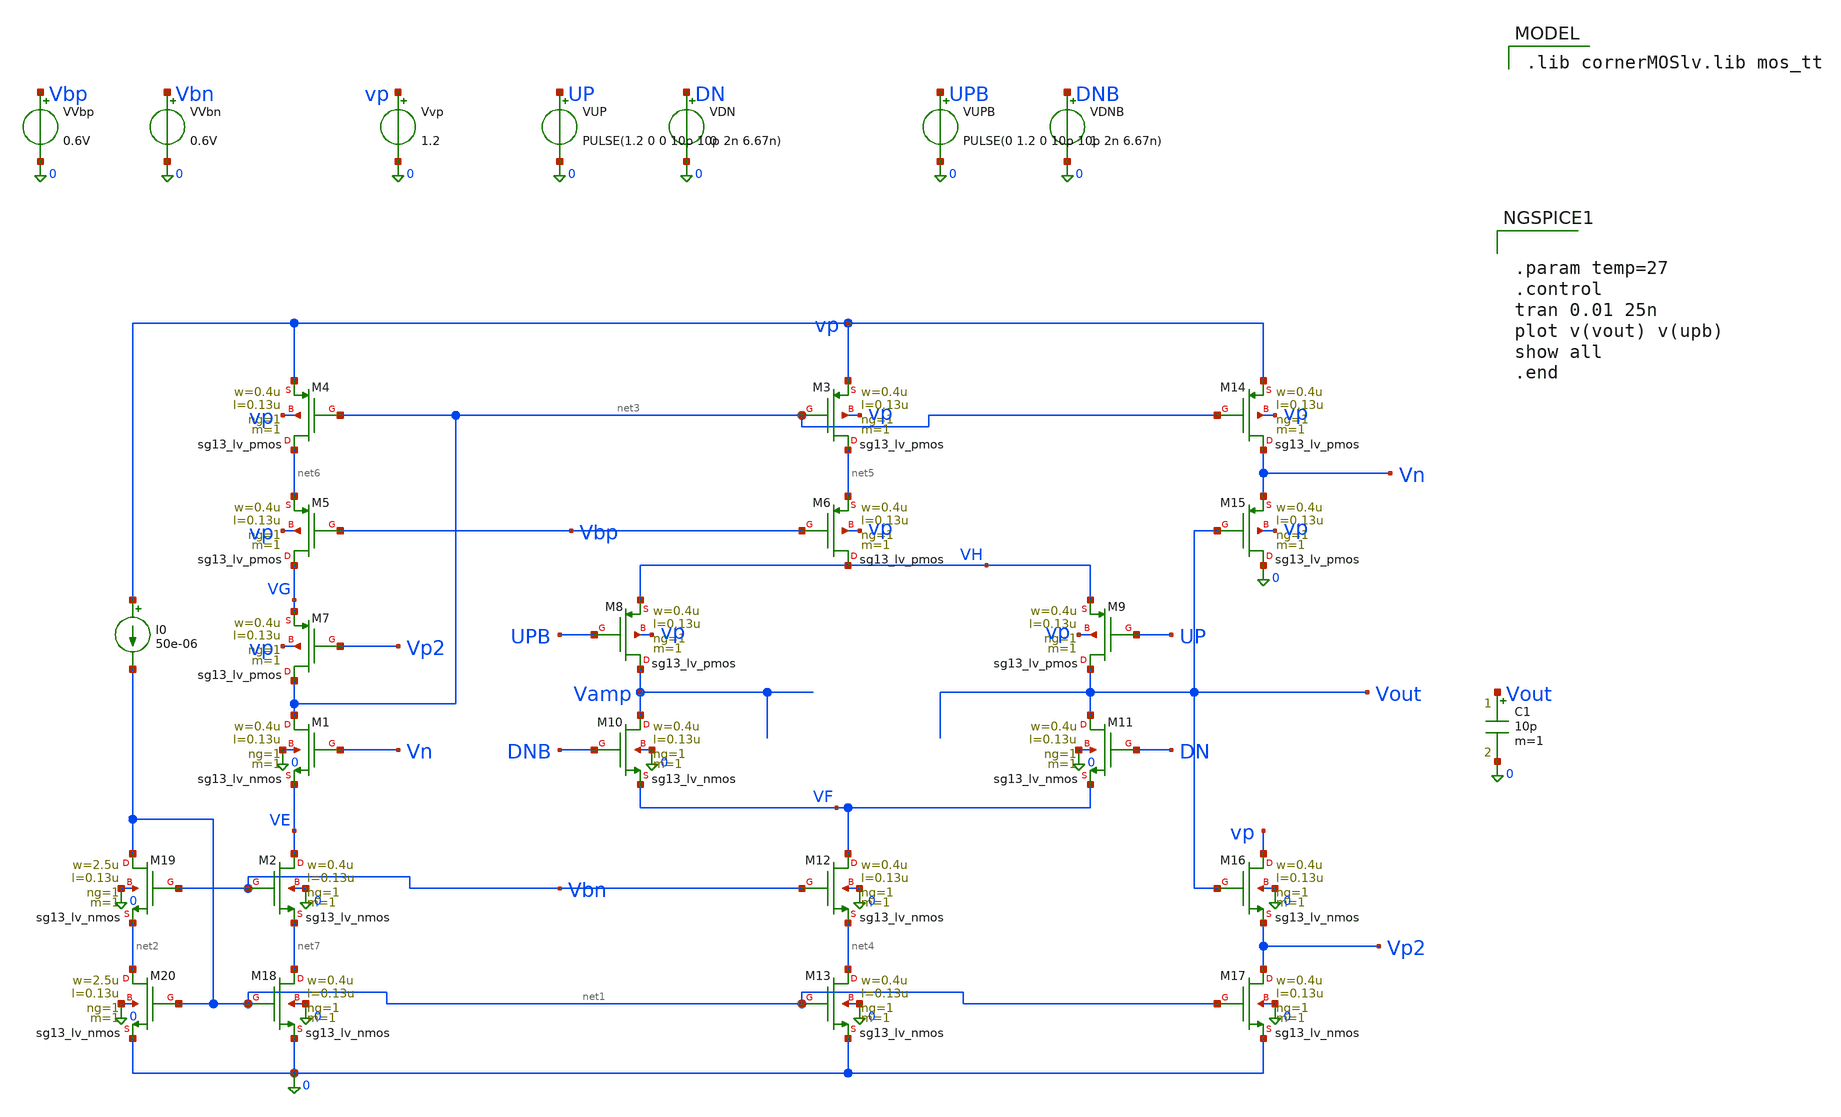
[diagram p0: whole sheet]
** sch_path: charge_pump/old_sch/cp_v2_tb (3).sch
**.subckt cp_v2_tb (3)
XM1 net3 Vn VE 0 sg13_lv_nmos w=0.4u l=0.13u ng=1 m=1 mm_ok=1
XM3 net5 net3 vp vp sg13_lv_pmos w=0.4u l=0.13u ng=1 m=1 mm_ok=1
XM4 net6 net3 vp vp sg13_lv_pmos w=0.4u l=0.13u ng=1 m=1 mm_ok=1
XM5 VG Vbp net6 vp sg13_lv_pmos w=0.4u l=0.13u ng=1 m=1 mm_ok=1
XM6 VH Vbp net5 vp sg13_lv_pmos w=0.4u l=0.13u ng=1 m=1 mm_ok=1
XM7 net3 Vp2 VG vp sg13_lv_pmos w=0.4u l=0.13u ng=1 m=1 mm_ok=1
XM8 Vamp UPB VH vp sg13_lv_pmos w=0.4u l=0.13u ng=1 m=1 mm_ok=1
XM9 Vout UP VH vp sg13_lv_pmos w=0.4u l=0.13u ng=1 m=1 mm_ok=1
XM10 Vamp DNB VF 0 sg13_lv_nmos w=0.4u l=0.13u ng=1 m=1 mm_ok=1
XM11 Vout DN VF 0 sg13_lv_nmos w=0.4u l=0.13u ng=1 m=1 mm_ok=1
XM12 VF Vbn net4 0 sg13_lv_nmos w=0.4u l=0.13u ng=1 m=1 mm_ok=1
XM13 net4 net1 0 0 sg13_lv_nmos w=0.4u l=0.13u ng=1 m=1 mm_ok=1
XM14 Vn net3 vp vp sg13_lv_pmos w=0.4u l=0.13u ng=1 m=1 mm_ok=1
XM15 0 Vout Vn vp sg13_lv_pmos w=0.4u l=0.13u ng=1 m=1 mm_ok=1
XM16 vp Vout Vp2 0 sg13_lv_nmos w=0.4u l=0.13u ng=1 m=1 mm_ok=1
XM17 Vp2 net1 0 0 sg13_lv_nmos w=0.4u l=0.13u ng=1 m=1 mm_ok=1
XM2 VE Vbn net7 0 sg13_lv_nmos w=0.4u l=0.13u ng=1 m=1 mm_ok=1
XM18 net7 net1 0 0 sg13_lv_nmos w=0.4u l=0.13u ng=1 m=1 mm_ok=1
XM19 net1 Vbn net2 0 sg13_lv_nmos w=2.5u l=0.13u ng=1 m=1 mm_ok=1
XM20 net2 net1 0 0 sg13_lv_nmos w=2.5u l=0.13u ng=1 m=1 mm_ok=1
I0 vp net1 50e-06
C1 Vout 0 10p m=1
Vvp vp 0 1.2
VUP UP 0 PULSE(1.2 0 0 10p 10p 2n 6.67n)
VDN DN 0 0
VVbp Vbp 0 0.6V
VVbn Vbn 0 0.6V
VUPB UPB 0 PULSE(0 1.2 0 10p 10p 2n 6.67n)
VDNB DNB 0 1
**** begin user architecture code
 .lib cornerMOSlv.lib mos_tt



.param temp=27
.control
tran 0.01 25n
plot v(vout) v(upb)
show all
.end


**** end user architecture code
**.ends
.end
